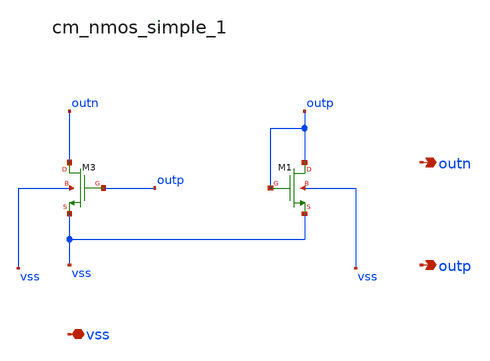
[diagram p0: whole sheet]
** sch_path: analog-db/raw/amp_024_smcnr/hier/blocks/cm_nmos_simple_1.sch
**.subckt cm_nmos_simple_1 vss outn outp
*.iopin vss
*.opin outn
*.opin outp
XM1 outp outp vss vss sg13_lv_nmos w=x_dut_xm1_w l=x_dut_xm1_l ng=1 m=x_dut_xm1_m
XM3 outn outp vss vss sg13_lv_nmos w=x_dut_xm3_w l=x_dut_xm3_l ng=1 m=x_dut_xm3_m
**.ends
.end
